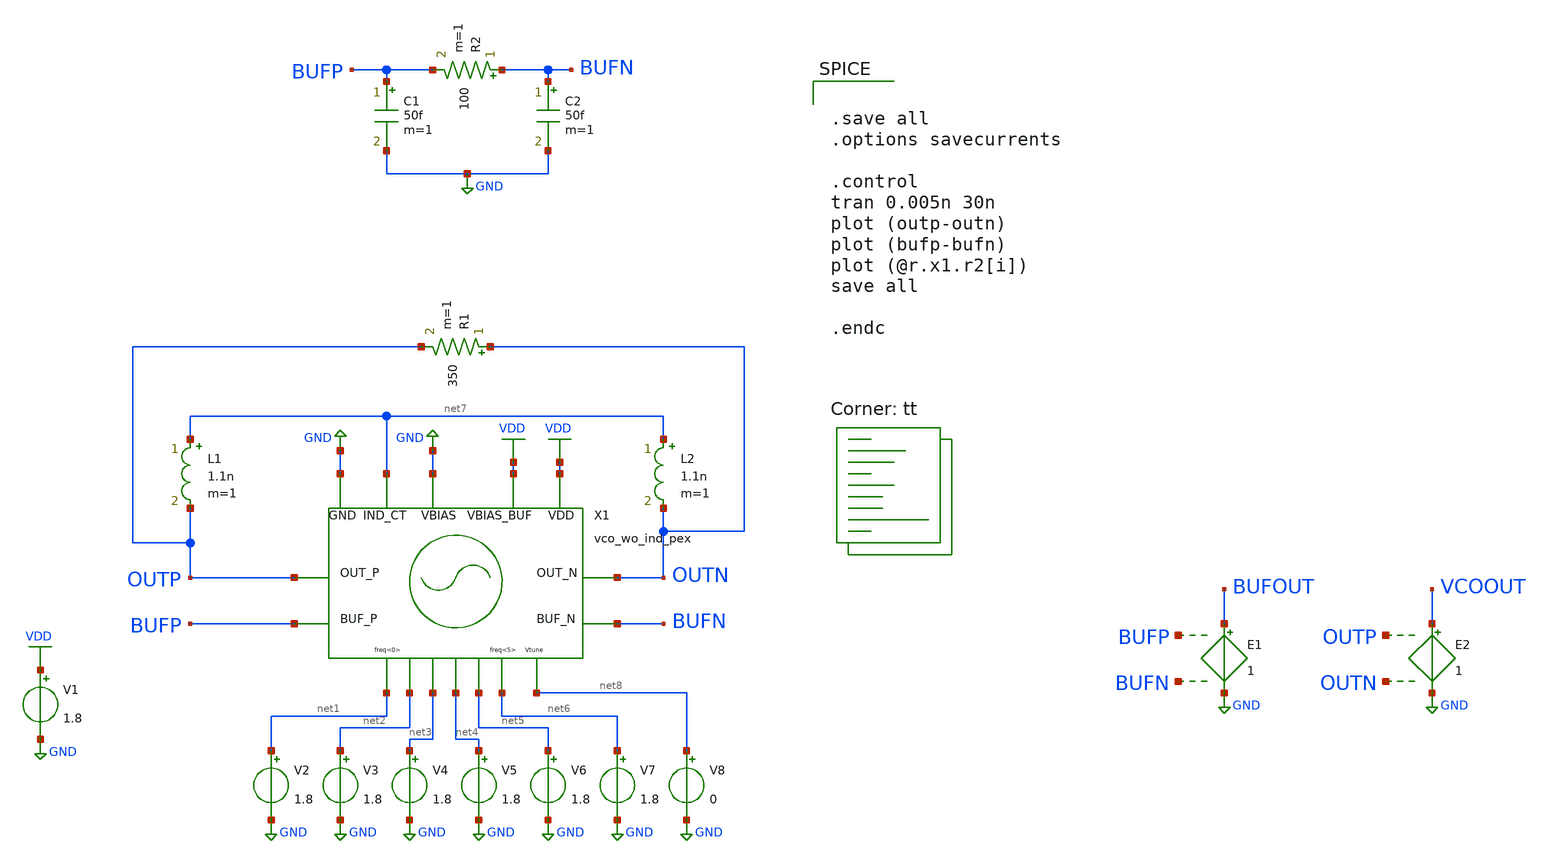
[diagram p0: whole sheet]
** sch_path: xschem/vco_wo_ind_pex_tb.sch
**.subckt vco_wo_ind_pex_tb
V1 VDD GND 1.8
V2 net1 GND 1.8
V3 net2 GND 1.8
V4 net3 GND 1.8
V5 net4 GND 1.8
V6 net5 GND 1.8
V7 net6 GND 1.8
L1 net7 OUTP 1.1n m=1
L2 net7 OUTN 1.1n m=1
V8 net8 GND 0
R1 OUTN OUTP 350 m=1
R2 BUFN BUFP 100 m=1
C1 BUFP GND 50f m=1
C2 BUFN GND 50f m=1
E1 BUFOUT GND BUFP BUFN 1
E2 VCOOUT GND OUTP OUTN 1
X1 OUTP GND net7 VDD OUTN net1 net2 net3 net4 net5 net6 GND net8 BUFP BUFN VDD vco_wo_ind_pex
**** begin user architecture code


.save all
.options savecurrents

.control
tran 0.005n 30n
plot (outp-outn)
plot (bufp-bufn)
plot (@r.x1.r2[i])
save all

.endc


.lib $::SKYWATER_MODELS/sky130.lib.spice tt
**** end user architecture code
**.ends
.GLOBAL GND
.GLOBAL VDD
.end
